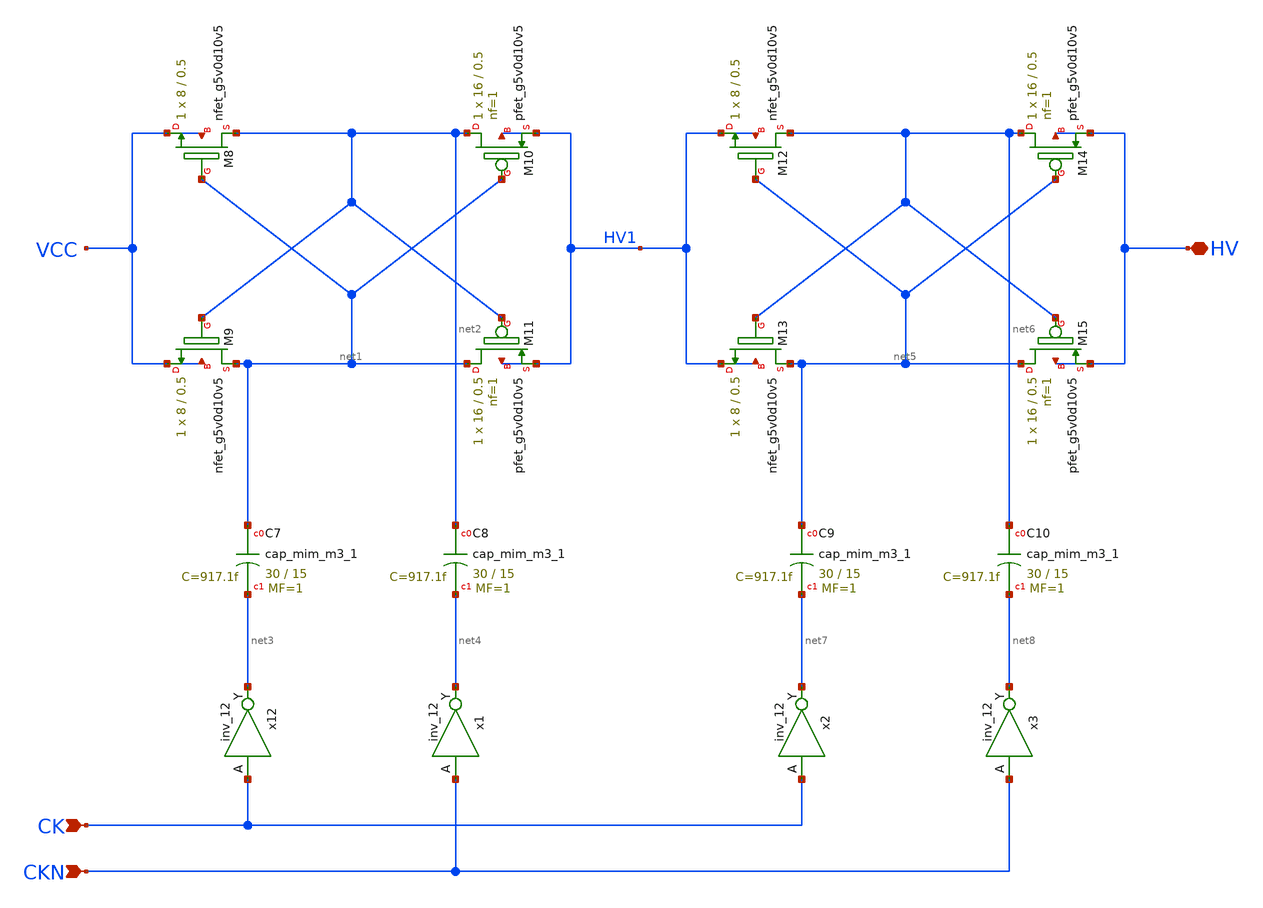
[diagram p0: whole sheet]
** sch_path: sky130_tests/charge_pump2.sch
**.subckt charge_pump2 HV CK CKN
*.iopin HV
*.ipin CK
*.ipin CKN
XM8 net2 net1 VCC VCC sky130_fd_pr__nfet_g5v0d10v5 W=8 L=0.5 ad='int((nf+1)/2) * W/nf * 0.29' pd='2*int((nf+1)/2) * (W/nf + 0.29)'
+ as='int((nf+2)/2) * W/nf * 0.29' ps='2*int((nf+2)/2) * (W/nf + 0.29)' nrd='0.29 / W' nrs='0.29 / W' sa=0
+ sb=0 sd=0 nf=1 mult=1
XM9 net1 net2 VCC VCC sky130_fd_pr__nfet_g5v0d10v5 W=8 L=0.5 ad='int((nf+1)/2) * W/nf * 0.29' pd='2*int((nf+1)/2) * (W/nf + 0.29)'
+ as='int((nf+2)/2) * W/nf * 0.29' ps='2*int((nf+2)/2) * (W/nf + 0.29)' nrd='0.29 / W' nrs='0.29 / W' sa=0
+ sb=0 sd=0 nf=1 mult=1
XM10 net2 net1 HV1 HV1 sky130_fd_pr__pfet_g5v0d10v5 L=0.5 W=16 nf=1 ad='int((nf+1)/2) * W/nf * 0.29'
+ as='int((nf+2)/2) * W/nf * 0.29' pd='2*int((nf+1)/2) * (W/nf + 0.29)' ps='2*int((nf+2)/2) * (W/nf + 0.29)'
+ nrd='0.29 / W' nrs='0.29 / W' sa=0 sb=0 sd=0 mult=1 m=1
XM11 net1 net2 HV1 HV1 sky130_fd_pr__pfet_g5v0d10v5 L=0.5 W=16 nf=1 ad='int((nf+1)/2) * W/nf * 0.29'
+ as='int((nf+2)/2) * W/nf * 0.29' pd='2*int((nf+1)/2) * (W/nf + 0.29)' ps='2*int((nf+2)/2) * (W/nf + 0.29)'
+ nrd='0.29 / W' nrs='0.29 / W' sa=0 sb=0 sd=0 mult=1 m=1
XC7 net1 net3 sky130_fd_pr__cap_mim_m3_1 W=30 L=15 MF=1 m=1
XC8 net2 net4 sky130_fd_pr__cap_mim_m3_1 W=30 L=15 MF=1 m=1
XM12 net6 net5 HV1 HV1 sky130_fd_pr__nfet_g5v0d10v5 W=8 L=0.5 ad='int((nf+1)/2) * W/nf * 0.29' pd='2*int((nf+1)/2) * (W/nf + 0.29)'
+ as='int((nf+2)/2) * W/nf * 0.29' ps='2*int((nf+2)/2) * (W/nf + 0.29)' nrd='0.29 / W' nrs='0.29 / W' sa=0
+ sb=0 sd=0 nf=1 mult=1
XM13 net5 net6 HV1 HV1 sky130_fd_pr__nfet_g5v0d10v5 W=8 L=0.5 ad='int((nf+1)/2) * W/nf * 0.29' pd='2*int((nf+1)/2) * (W/nf + 0.29)'
+ as='int((nf+2)/2) * W/nf * 0.29' ps='2*int((nf+2)/2) * (W/nf + 0.29)' nrd='0.29 / W' nrs='0.29 / W' sa=0
+ sb=0 sd=0 nf=1 mult=1
XM14 net6 net5 HV HV sky130_fd_pr__pfet_g5v0d10v5 L=0.5 W=16 nf=1 ad='int((nf+1)/2) * W/nf * 0.29' as='int((nf+2)/2) * W/nf * 0.29'
+ pd='2*int((nf+1)/2) * (W/nf + 0.29)' ps='2*int((nf+2)/2) * (W/nf + 0.29)' nrd='0.29 / W' nrs='0.29 / W'
+ sa=0 sb=0 sd=0 mult=1 m=1
XM15 net5 net6 HV HV sky130_fd_pr__pfet_g5v0d10v5 L=0.5 W=16 nf=1 ad='int((nf+1)/2) * W/nf * 0.29' as='int((nf+2)/2) * W/nf * 0.29'
+ pd='2*int((nf+1)/2) * (W/nf + 0.29)' ps='2*int((nf+2)/2) * (W/nf + 0.29)' nrd='0.29 / W' nrs='0.29 / W'
+ sa=0 sb=0 sd=0 mult=1 m=1
XC9 net5 net7 sky130_fd_pr__cap_mim_m3_1 W=30 L=15 MF=1 m=1
XC10 net6 net8 sky130_fd_pr__cap_mim_m3_1 W=30 L=15 MF=1 m=1
x12 CK GND GND VCC VCC net3 sky130_fd_sc_hd__inv_12
x1 CKN GND GND VCC VCC net4 sky130_fd_sc_hd__inv_12
x2 CK GND GND VCC VCC net7 sky130_fd_sc_hd__inv_12
x3 CKN GND GND VCC VCC net8 sky130_fd_sc_hd__inv_12
**.ends
.end
